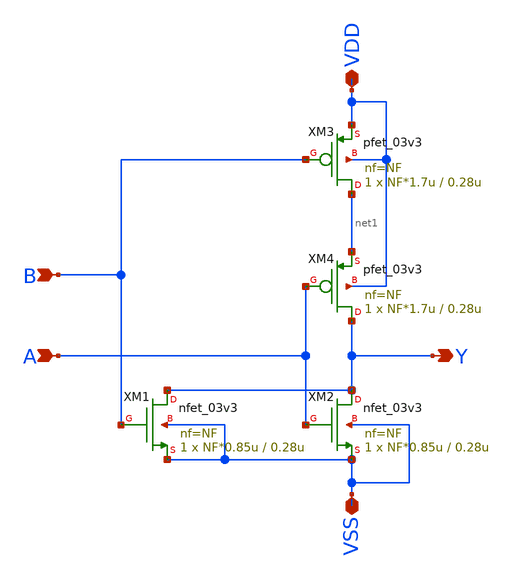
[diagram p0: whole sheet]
** sch_path: xschem_lib/DFFRAM_full_custom/nor.sch
**.subckt nor VDD VSS Y A B
*.iopin VDD
*.iopin VSS
*.opin Y
*.ipin A
*.ipin B
XM3 net1 B VDD VDD pfet_03v3 L=0.28u W=NF*1.7u nf=NF ad='int((nf+1)/2) * W/nf * 0.18u' as='int((nf+2)/2) * W/nf * 0.18u'
+ pd='2*int((nf+1)/2) * (W/nf + 0.18u)' ps='2*int((nf+2)/2) * (W/nf + 0.18u)' nrd='0.18u / W' nrs='0.18u / W'
+ sa=0 sb=0 sd=0 m=1
XM4 Y A net1 VDD pfet_03v3 L=0.28u W=NF*1.7u nf=NF ad='int((nf+1)/2) * W/nf * 0.18u' as='int((nf+2)/2) * W/nf * 0.18u'
+ pd='2*int((nf+1)/2) * (W/nf + 0.18u)' ps='2*int((nf+2)/2) * (W/nf + 0.18u)' nrd='0.18u / W' nrs='0.18u / W'
+ sa=0 sb=0 sd=0 m=1
XM1 Y B VSS VSS nfet_03v3 L=0.28u W=NF*0.85u nf=NF ad='int((nf+1)/2) * W/nf * 0.18u' as='int((nf+2)/2) * W/nf * 0.18u'
+ pd='2*int((nf+1)/2) * (W/nf + 0.18u)' ps='2*int((nf+2)/2) * (W/nf + 0.18u)' nrd='0.18u / W' nrs='0.18u / W'
+ sa=0 sb=0 sd=0 m=1
XM2 Y A VSS VSS nfet_03v3 L=0.28u W=NF*0.85u nf=NF ad='int((nf+1)/2) * W/nf * 0.18u' as='int((nf+2)/2) * W/nf * 0.18u'
+ pd='2*int((nf+1)/2) * (W/nf + 0.18u)' ps='2*int((nf+2)/2) * (W/nf + 0.18u)' nrd='0.18u / W' nrs='0.18u / W'
+ sa=0 sb=0 sd=0 m=1
**.ends
.end
